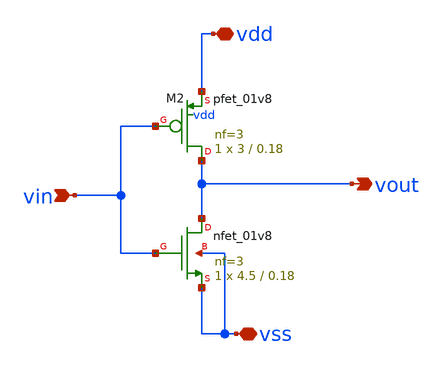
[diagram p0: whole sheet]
** sch_path: ubntu_files/xschem/inverter.sch
**.subckt inverter vin vdd vss vout
*.ipin vin
*.iopin vdd
*.iopin vss
*.opin vout
XM1 vout vin vss vss sky130_fd_pr__nfet_01v8 L=0.18 W=4.5 nf=3 ad= 'int((nf+1)/2) * W/nf * 0.29' as=
+ 'int((nf+2)/2) * W/nf * 0.29' pd= '2*int((nf+1)/2) * (W/nf + 0.29)' ps= '2*int((nf+2)/2) * (W/nf + 0.29)'
+ nrd= '0.29 / W' nrs= '0.29 / W' sa=0 sb=0 sd=0 mult=1 m=1
XM2 vout vin vdd vdd sky130_fd_pr__pfet_01v8 L=0.18 W=3 nf=3 ad= 'int((nf+1)/2) * W/nf * 0.29' as= 'int((nf+2)/2) * W/nf * 0.29'
+ pd= '2*int((nf+1)/2) * (W/nf + 0.29)' ps= '2*int((nf+2)/2) * (W/nf + 0.29)' nrd= '0.29 / W' nrs= '0.29 / W'
+ sa=0 sb=0 sd=0 mult=1 m=1
**.ends
.end
